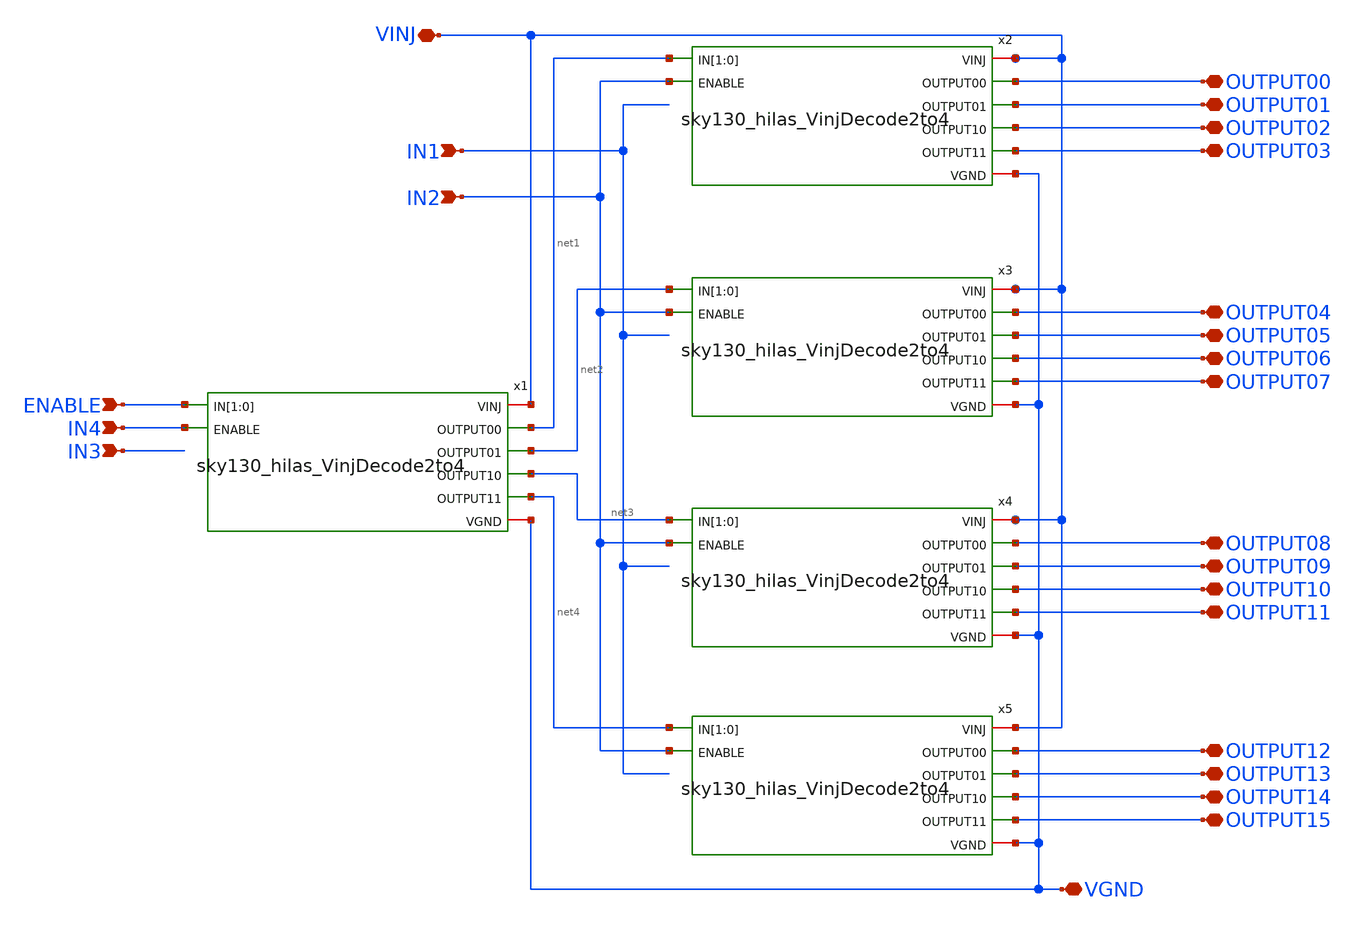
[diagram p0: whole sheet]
** sch_path: sky130_cells/RDAC/Design/sky130_hilas_Vinj_Decode_4to16.sch
**.subckt sky130_hilas_Vinj_Decode_4to16 ENABLE IN1 IN2 IN3 IN4 VGND OUTPUT00 OUTPUT01 OUTPUT02
*+ OUTPUT03 OUTPUT04 OUTPUT05 OUTPUT06 OUTPUT07 OUTPUT08 OUTPUT09 OUTPUT10 OUTPUT11 OUTPUT12 OUTPUT13 OUTPUT14
*+ OUTPUT15 VINJ
*.ipin ENABLE
*.ipin IN1
*.ipin IN2
*.ipin IN3
*.ipin IN4
*.iopin VGND
*.iopin OUTPUT00
*.iopin OUTPUT01
*.iopin OUTPUT02
*.iopin OUTPUT03
*.iopin OUTPUT04
*.iopin OUTPUT05
*.iopin OUTPUT06
*.iopin OUTPUT07
*.iopin OUTPUT08
*.iopin OUTPUT09
*.iopin OUTPUT10
*.iopin OUTPUT11
*.iopin OUTPUT12
*.iopin OUTPUT13
*.iopin OUTPUT14
*.iopin OUTPUT15
*.iopin VINJ
x1 VINJ ENABLE ENABLE IN4 net1 net2 net3 net4 VGND sky130_hilas_VinjDecode2to4
x2 VINJ net1 net1 IN2 OUTPUT00 OUTPUT01 OUTPUT02 OUTPUT03 VGND sky130_hilas_VinjDecode2to4
x3 VINJ net2 net2 IN2 OUTPUT04 OUTPUT05 OUTPUT06 OUTPUT07 VGND sky130_hilas_VinjDecode2to4
x4 VINJ net3 net3 IN2 OUTPUT08 OUTPUT09 OUTPUT10 OUTPUT11 VGND sky130_hilas_VinjDecode2to4
x5 VINJ net4 net4 IN2 OUTPUT12 OUTPUT13 OUTPUT14 OUTPUT15 VGND sky130_hilas_VinjDecode2to4
**.ends

* expanding   symbol:  sky130_cells/RDAC/Design/sky130_hilas_VinjDecode2to4.sym # of pins=8
** sym_path: sky130_cells/RDAC/Design/sky130_hilas_VinjDecode2to4.sym
** sch_path: sky130_cells/RDAC/Design/sky130_hilas_VinjDecode2to4.sch
.subckt sky130_hilas_VinjDecode2to4 VINJ IN[1] IN[0] ENABLE OUTPUT00 OUTPUT01 OUTPUT10 OUTPUT11 VGND
*.ipin ENABLE
*.opin OUTPUT00
*.opin OUTPUT01
*.opin OUTPUT10
*.opin OUTPUT11
*.iopin VINJ
*.iopin VGND
*.ipin IN[1],IN[0]
x2 VINJ IN[1] VinjNOR3_2/Input2 VGND sky130_hilas_VinjInv2
x3 VINJ IN[0] VinjNOR3_1/Input1 VGND sky130_hilas_VinjInv2
x4 VINJ ENABLE VinjNOR3_3/Input3 VGND sky130_hilas_VinjInv2
x1 VINJ IN[1] IN[0] VinjNOR3_3/Input3 OUTPUT00 VGND sky130_hilas_VinjNOR3
x5 VINJ IN[1] VinjNOR3_1/Input1 VinjNOR3_3/Input3 OUTPUT01 VGND sky130_hilas_VinjNOR3
x6 VINJ VinjNOR3_2/Input2 IN[0] VinjNOR3_3/Input3 OUTPUT10 VGND sky130_hilas_VinjNOR3
x7 VINJ VinjNOR3_2/Input2 VinjNOR3_1/Input1 VinjNOR3_3/Input3 OUTPUT11 VGND sky130_hilas_VinjNOR3
.ends


* expanding   symbol:  sky130_cells/RDAC/Design/sky130_hilas_VinjInv2.sym # of pins=4
** sym_path: sky130_cells/RDAC/Design/sky130_hilas_VinjInv2.sym
** sch_path: sky130_cells/RDAC/Design/sky130_hilas_VinjInv2.sch
.subckt sky130_hilas_VinjInv2 Vinj Input Output GND
*.ipin Input
*.opin Output
*.iopin Vinj
*.iopin GND
XM4 Output Input Vinj Vinj sky130_fd_pr__pfet_g5v0d10v5 L=0.53 W=0.42 nf=1 ad='int((nf+1)/2) * W/nf * 0.29'
+ as='int((nf+2)/2) * W/nf * 0.29' pd='2*int((nf+1)/2) * (W/nf + 0.29)' ps='2*int((nf+2)/2) * (W/nf + 0.29)'
+ nrd='0.29 / W' nrs='0.29 / W' sa=0 sb=0 sd=0 mult=1 m=1
XM3 Output Input GND GND sky130_fd_pr__nfet_g5v0d10v5 L=0.52 W=0.42 nf=1 ad='int((nf+1)/2) * W/nf * 0.29'
+ as='int((nf+2)/2) * W/nf * 0.29' pd='2*int((nf+1)/2) * (W/nf + 0.29)' ps='2*int((nf+2)/2) * (W/nf + 0.29)'
+ nrd='0.29 / W' nrs='0.29 / W' sa=0 sb=0 sd=0 mult=1 m=1
.ends


* expanding   symbol:  sky130_cells/RDAC/Design/sky130_hilas_VinjNOR3.sym # of pins=6
** sym_path: sky130_cells/RDAC/Design/sky130_hilas_VinjNOR3.sym
** sch_path: sky130_cells/RDAC/Design/sky130_hilas_VinjNOR3.sch
.subckt sky130_hilas_VinjNOR3 Vinj Input1 Input2 Input3 OUTPUT GND
*.ipin Input3
*.ipin Input1
*.ipin Input2
*.iopin Vinj
*.iopin GND
*.opin OUTPUT
XM1 OUTPUT Input3 GND GND sky130_fd_pr__nfet_g5v0d10v5 L=0.5 W=0.42 nf=1 ad='int((nf+1)/2) * W/nf * 0.29'
+ as='int((nf+2)/2) * W/nf * 0.29' pd='2*int((nf+1)/2) * (W/nf + 0.29)' ps='2*int((nf+2)/2) * (W/nf + 0.29)'
+ nrd='0.29 / W' nrs='0.29 / W' sa=0 sb=0 sd=0 mult=1 m=1
XM2 OUTPUT Input1 GND GND sky130_fd_pr__nfet_g5v0d10v5 L=0.51 W=0.43 nf=1 ad='int((nf+1)/2) * W/nf * 0.29'
+ as='int((nf+2)/2) * W/nf * 0.29' pd='2*int((nf+1)/2) * (W/nf + 0.29)' ps='2*int((nf+2)/2) * (W/nf + 0.29)'
+ nrd='0.29 / W' nrs='0.29 / W' sa=0 sb=0 sd=0 mult=1 m=1
XM3 OUTPUT Input2 GND GND sky130_fd_pr__nfet_g5v0d10v5 L=0.5 W=0.42 nf=1 ad='int((nf+1)/2) * W/nf * 0.29'
+ as='int((nf+2)/2) * W/nf * 0.29' pd='2*int((nf+1)/2) * (W/nf + 0.29)' ps='2*int((nf+2)/2) * (W/nf + 0.29)'
+ nrd='0.29 / W' nrs='0.29 / W' sa=0 sb=0 sd=0 mult=1 m=1
XM6 OUTPUT Input2 net2 Vinj sky130_fd_pr__pfet_g5v0d10v5 L=0.52 W=0.43 nf=1 ad='int((nf+1)/2) * W/nf * 0.29'
+ as='int((nf+2)/2) * W/nf * 0.29' pd='2*int((nf+1)/2) * (W/nf + 0.29)' ps='2*int((nf+2)/2) * (W/nf + 0.29)'
+ nrd='0.29 / W' nrs='0.29 / W' sa=0 sb=0 sd=0 mult=1 m=1
XM4 net2 Input1 net1 Vinj sky130_fd_pr__pfet_g5v0d10v5 L=0.52 W=0.42 nf=1 ad='int((nf+1)/2) * W/nf * 0.29'
+ as='int((nf+2)/2) * W/nf * 0.29' pd='2*int((nf+1)/2) * (W/nf + 0.29)' ps='2*int((nf+2)/2) * (W/nf + 0.29)'
+ nrd='0.29 / W' nrs='0.29 / W' sa=0 sb=0 sd=0 mult=1 m=1
XM5 net1 Input3 Vinj Vinj sky130_fd_pr__pfet_g5v0d10v5 L=0.53 W=0.42 nf=1 ad='int((nf+1)/2) * W/nf * 0.29'
+ as='int((nf+2)/2) * W/nf * 0.29' pd='2*int((nf+1)/2) * (W/nf + 0.29)' ps='2*int((nf+2)/2) * (W/nf + 0.29)'
+ nrd='0.29 / W' nrs='0.29 / W' sa=0 sb=0 sd=0 mult=1 m=1
.ends

.end
